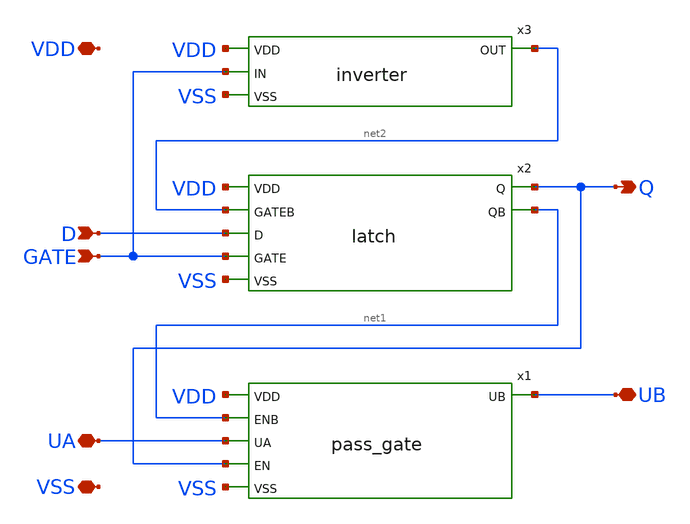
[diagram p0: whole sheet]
** sch_path: xschem/latched_switch.sch
**.subckt latched_switch VSS UB VDD UA D GATE Q
*.iopin VSS
*.iopin UB
*.iopin VDD
*.iopin UA
*.ipin D
*.ipin GATE
*.opin Q
x1 VDD net1 UA UB Q VSS pass_gate
x2 Q VDD net1 net2 D GATE VSS latch
x3 VDD GATE net2 VSS inverter
**.ends
.end
